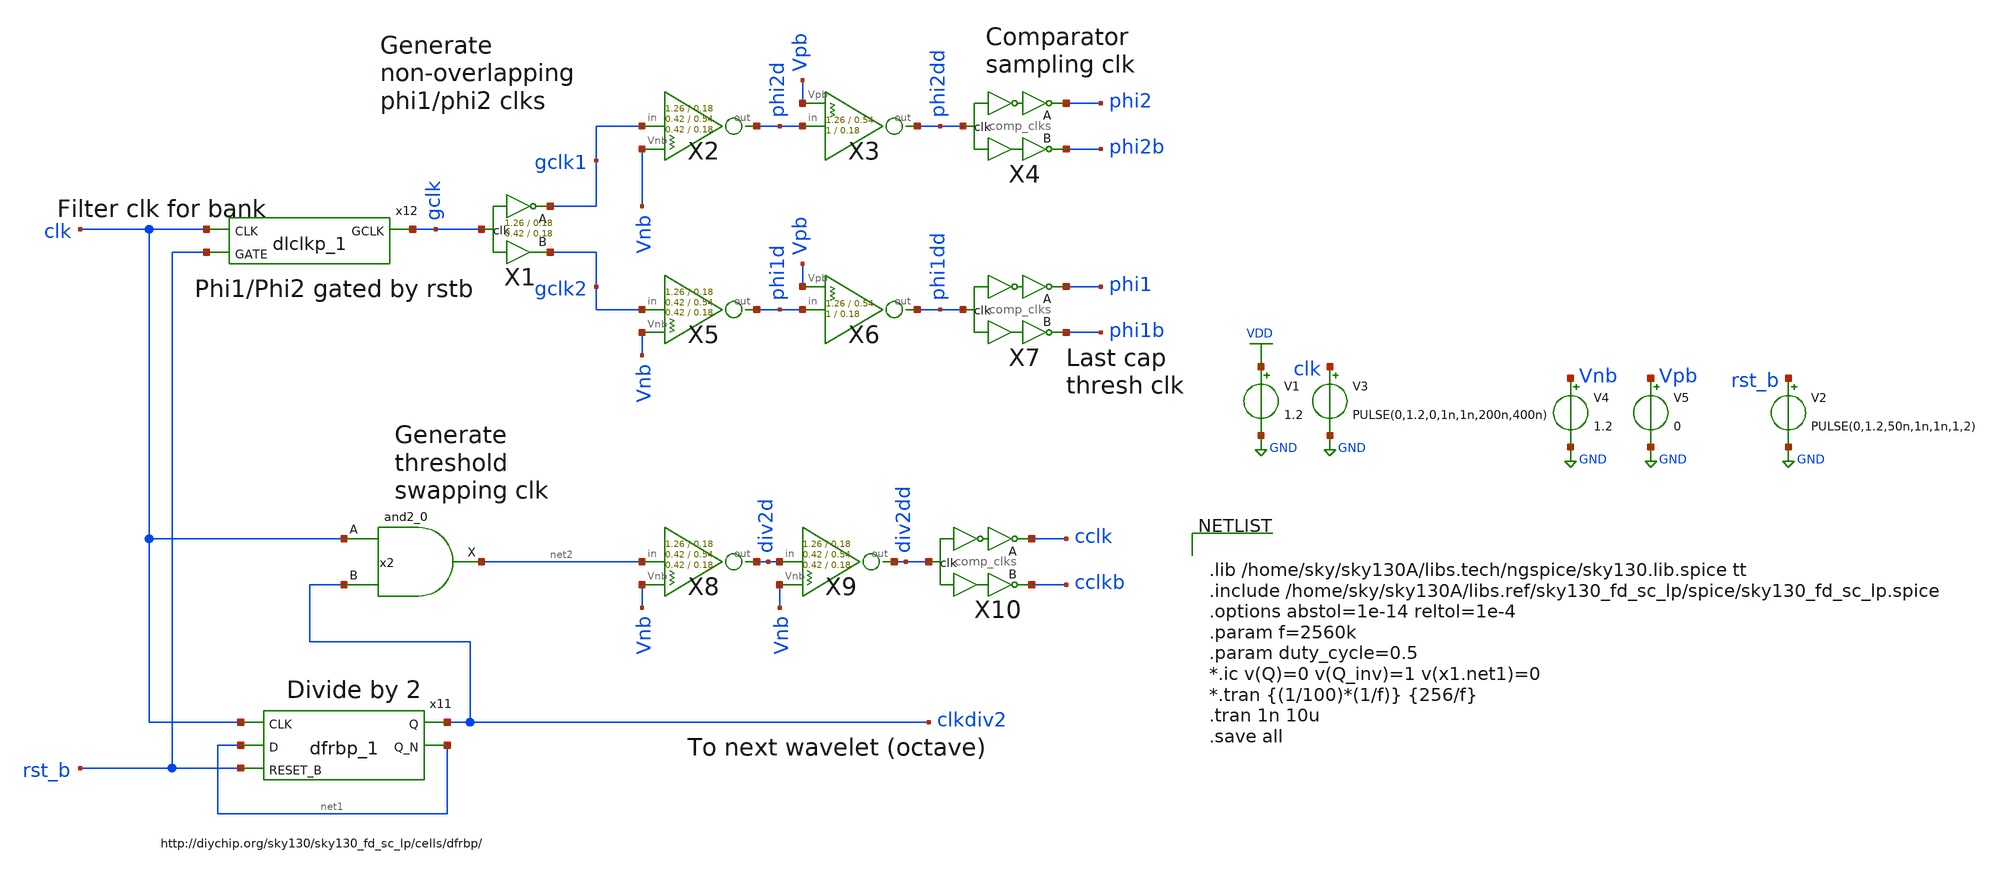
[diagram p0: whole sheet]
** sch_path: xschem/comparator_with_AZ/clk_div2.sch
**.subckt clk_div2
V1 VDD GND 1.2
V3 clk GND PULSE(0,1.2,0,1n,1n,200n,400n)
x11 clk net1 rst_b gnd gnd vdd vdd clkdiv2 net1 sky130_fd_sc_lp__dfrbp_1
X4 phi2dd phi2 phi2b comp_clks Wpmos=1.26 Lpmos=0.18 Wnmos=0.42 Lnmos=0.18
X7 phi1dd phi1 phi1b comp_clks Wpmos=1.26 Lpmos=0.18 Wnmos=0.42 Lnmos=0.18
X10 div2dd cclk cclkb comp_clks Wpmos=1.26 Lpmos=0.18 Wnmos=0.42 Lnmos=0.18
x12 clk rst_b gnd gnd vdd vdd gclk sky130_fd_sc_lp__dlclkp_1
X1 gclk gclk1 gclk2 comp_clks_1stage Wpmos=1.26 Lpmos=0.18 Wnmos=0.42 Lnmos=0.18
x2 clk clkdiv2 gnd gnd vdd vdd net2 sky130_fd_sc_lp__and2_0
X2 gclk1 phi2d Vnb inv_weak_pulldown Wpmos=1.26 Lpmos= Wnmos= Lnmos=0.54
X5 gclk2 phi1d Vnb inv_weak_pulldown Wpmos=1.26 Lpmos= Wnmos= Lnmos=0.54
X8 net2 div2d Vnb inv_weak_pulldown Wpmos=1.26 Lpmos= Wnmos= Lnmos=0.54
X9 div2d div2dd Vnb inv_weak_pulldown Wpmos=1.26 Lpmos= Wnmos= Lnmos=0.54
X3 phi2d phi2dd Vpb inv_weak_pullup Wpmos=1.26 Lpmos=0.54 Wnmos=1 Lnmos=0.18
X6 phi1d phi1dd Vpb inv_weak_pullup Wpmos=1.26 Lpmos=0.54 Wnmos=1 Lnmos=0.18
V2 rst_b GND PULSE(0,1.2,50n,1n,1n,1,2)
V4 Vnb GND 1.2
V5 Vpb GND 0
**** begin user architecture code


.lib /home/sky/sky130A/libs.tech/ngspice/sky130.lib.spice tt
.include /home/sky/sky130A/libs.ref/sky130_fd_sc_lp/spice/sky130_fd_sc_lp.spice
.options abstol=1e-14 reltol=1e-4
.param f=2560k
.param duty_cycle=0.5
*.ic v(Q)=0 v(Q_inv)=1 v(x1.net1)=0
*.tran {(1/100)*(1/f)} {256/f}
.tran 1n 10u
.save all


**** end user architecture code
**.ends
.GLOBAL GND
.GLOBAL VDD
.end
